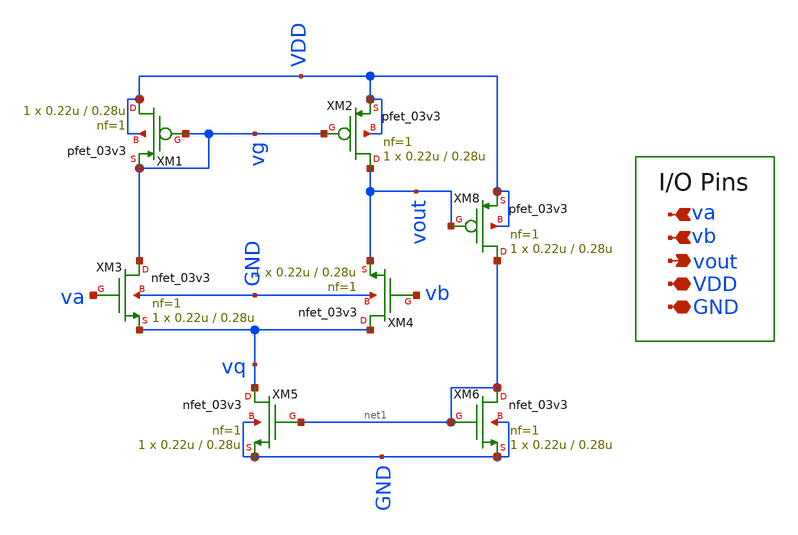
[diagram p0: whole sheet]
** sch_path: gf180_amplifier_with_bias-ckt.sch
**.subckt gf180_amplifier_with_bias-ckt va VDD vb vout GND
*.ipin va
*.iopin VDD
*.ipin vb
*.opin vout
*.iopin GND
XM1 VDD vg vg VDD pfet_03v3 L=0.28u W=0.22u nf=1 ad='int((nf+1)/2) * W/nf * 0.18u' as='int((nf+2)/2) * W/nf * 0.18u'
+ pd='2*int((nf+1)/2) * (W/nf + 0.18u)' ps='2*int((nf+2)/2) * (W/nf + 0.18u)' nrd='0.18u / W' nrs='0.18u / W'
+ sa=0 sb=0 sd=0 m=1
XM2 vout vg VDD VDD pfet_03v3 L=0.28u W=0.22u nf=1 ad='int((nf+1)/2) * W/nf * 0.18u' as='int((nf+2)/2) * W/nf * 0.18u'
+ pd='2*int((nf+1)/2) * (W/nf + 0.18u)' ps='2*int((nf+2)/2) * (W/nf + 0.18u)' nrd='0.18u / W' nrs='0.18u / W'
+ sa=0 sb=0 sd=0 m=1
XM3 vg va vq GND nfet_03v3 L=0.28u W=0.22u nf=1 ad='int((nf+1)/2) * W/nf * 0.18u' as='int((nf+2)/2) * W/nf * 0.18u'
+ pd='2*int((nf+1)/2) * (W/nf + 0.18u)' ps='2*int((nf+2)/2) * (W/nf + 0.18u)' nrd='0.18u / W' nrs='0.18u / W'
+ sa=0 sb=0 sd=0 m=1
XM4 vq vb vout GND nfet_03v3 L=0.28u W=0.22u nf=1 ad='int((nf+1)/2) * W/nf * 0.18u' as='int((nf+2)/2) * W/nf * 0.18u'
+ pd='2*int((nf+1)/2) * (W/nf + 0.18u)' ps='2*int((nf+2)/2) * (W/nf + 0.18u)' nrd='0.18u / W' nrs='0.18u / W'
+ sa=0 sb=0 sd=0 m=1
XM5 vq net1 GND GND nfet_03v3 L=0.28u W=0.22u nf=1 ad='int((nf+1)/2) * W/nf * 0.18u' as='int((nf+2)/2) * W/nf * 0.18u'
+ pd='2*int((nf+1)/2) * (W/nf + 0.18u)' ps='2*int((nf+2)/2) * (W/nf + 0.18u)' nrd='0.18u / W' nrs='0.18u / W'
+ sa=0 sb=0 sd=0 m=1
XM6 net1 net1 GND GND nfet_03v3 L=0.28u W=0.22u nf=1 ad='int((nf+1)/2) * W/nf * 0.18u' as='int((nf+2)/2) * W/nf * 0.18u'
+ pd='2*int((nf+1)/2) * (W/nf + 0.18u)' ps='2*int((nf+2)/2) * (W/nf + 0.18u)' nrd='0.18u / W' nrs='0.18u / W'
+ sa=0 sb=0 sd=0 m=1
XM8 net1 vout VDD VDD pfet_03v3 L=0.28u W=0.22u nf=1 ad='int((nf+1)/2) * W/nf * 0.18u' as='int((nf+2)/2) * W/nf * 0.18u'
+ pd='2*int((nf+1)/2) * (W/nf + 0.18u)' ps='2*int((nf+2)/2) * (W/nf + 0.18u)' nrd='0.18u / W' nrs='0.18u / W'
+ sa=0 sb=0 sd=0 m=1
**.ends
.end
